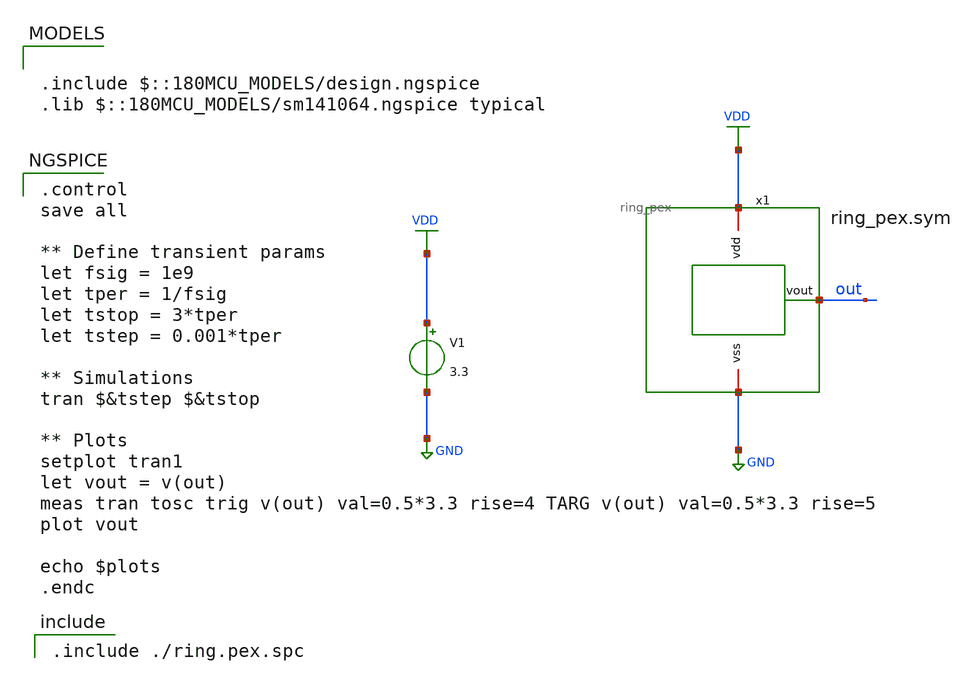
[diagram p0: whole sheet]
** sch_path: gf180-2025/ring/ring_pex_tb.sch
**.subckt ring_pex_tb
V1 VDD GND 3.3
x1 VDD out GND ring_pex
**** begin user architecture code

.include $::180MCU_MODELS/design.ngspice
.lib $::180MCU_MODELS/sm141064.ngspice typical


.control
save all

** Define transient params
let fsig = 1e9
let tper = 1/fsig
let tstop = 3*tper
let tstep = 0.001*tper

** Simulations
tran $&tstep $&tstop

** Plots
setplot tran1
let vout = v(out)
meas tran tosc trig v(out) val=0.5*3.3 rise=4 TARG v(out) val=0.5*3.3 rise=5
plot vout

echo $plots
.endc



.include ./ring.pex.spc

**** end user architecture code
**.ends
.GLOBAL VDD
.GLOBAL GND
.end
